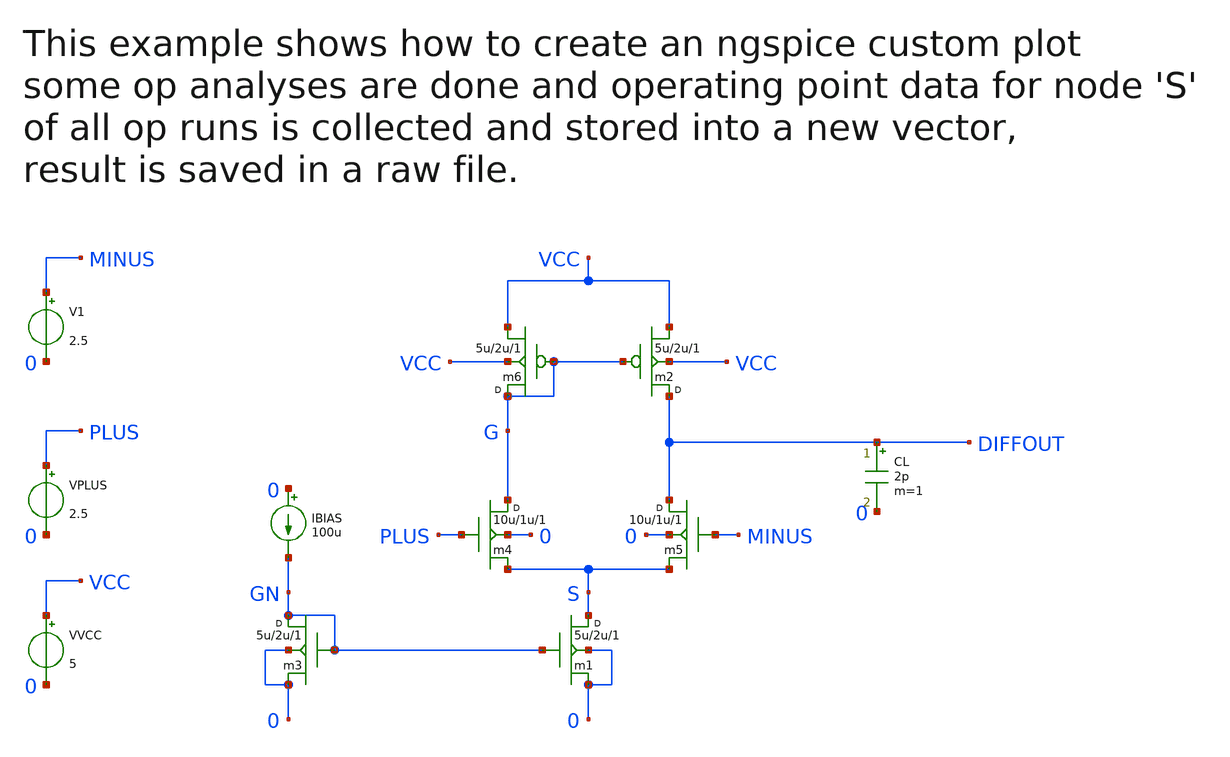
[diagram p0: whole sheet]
** sch_path: xschem_libs_newsym/examples/plot_manipulation/schematic/plot_manipulation.sch
* Copyright (C) 1998-2024 Stefan Frederik Schippers
* This program is free software; you can redistribute it and/or modify
* it under the terms of the GNU General Public License as published by
* the Free Software Foundation; either version 2 of the License, or
* (at your option) any later version.
* This program is distributed in the hope that it will be useful,
* but WITHOUT ANY WARRANTY; without even the implied warranty of
* MERCHANTABILITY or FITNESS FOR A PARTICULAR PURPOSE.  See the
* GNU General Public License for more details.
* You should have received a copy of the GNU General Public License
* along with this program; if not, write to the Free Software
**.subckt plot_manipulation
m1 S GN 0 0 cmosn w=5u l=2u m=1
m2 DIFFOUT G VCC VCC cmosp w=5u l=2u m=1
VVCC VCC 0 5
m3 GN GN 0 0 cmosn w=5u l=2u m=1
IBIAS 0 GN 100u
m4 G PLUS S 0 cmosn w=10u l=1u m=1
m5 DIFFOUT MINUS S 0 cmosn w=10u l=1u m=1
m6 G G VCC VCC cmosp w=5u l=2u m=1
VPLUS PLUS 0 2.5
V1 MINUS 0 2.5
CL DIFFOUT 0 2p m=1
**** begin user architecture code


** ngspice
.temp 30

** xyce
* .step temp list 30

** ngspice
* .save all

** models are generally not free: you must download
** SPICE models for active devices and put them  into the below
** referenced file in netlist/simulation directory.
.option savecurrents
.include "models_cmos_example.txt"
.control
save all
let vol = 0
let i = 1
set curplot = new         $ create a new plot
set myplot = $curplot     $ store the plot name
set curplotname = myplot
let s_vec = vector(61)
settype voltage s_vec
while vol <= 6
alter VVCC vol  $ change value of vcc source
op
let vol = vol + 0.1
set run = $&i  $ create a var from the vector
let i = i + 1
setplot $myplot
let s_vec[{$run}] = op{$run}.s  $ get operating point v(s) and store into vector
end
* current plot here is last set one, $myplot
compose vcc start=0 stop=6 step=0.1  $ build x-axis voltage
setscale vcc                         $ set as xaxis for myplot
settype voltage vcc
write plot_manipulation.raw
plot s_vec
quit 0
.endc

** ngspice
* .save all

** xyce, not needed if -r given om cmdline
* .print tran format=raw v(diffout) v(plus) v(minus)


**** end user architecture code
**.ends
.end
